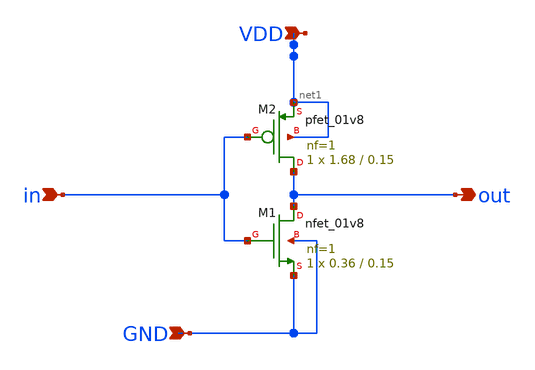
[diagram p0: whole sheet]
** sch_path: closed_loop_symbol_view_simulation/inv_buf.sch
**.subckt inv_buf out in VDD GND
*.opin out
*.ipin in
*.ipin VDD
*.ipin GND
XM2 out in net1 net1 sky130_fd_pr__pfet_01v8 L=0.15 W=1.68 nf=1 ad='int((nf+1)/2) * W/nf * 0.29' as='int((nf+2)/2) * W/nf * 0.29'
+ pd='2*int((nf+1)/2) * (W/nf + 0.29)' ps='2*int((nf+2)/2) * (W/nf + 0.29)' nrd='0.29 / W' nrs='0.29 / W'
+ sa=0 sb=0 sd=0 mult=1 m=1
XM1 out in GND GND sky130_fd_pr__nfet_01v8 L=0.15 W=0.36 nf=1 ad='int((nf+1)/2) * W/nf * 0.29' as='int((nf+2)/2) * W/nf * 0.29'
+ pd='2*int((nf+1)/2) * (W/nf + 0.29)' ps='2*int((nf+2)/2) * (W/nf + 0.29)' nrd='0.29 / W' nrs='0.29 / W'
+ sa=0 sb=0 sd=0 mult=1 m=1
**.ends
.end
